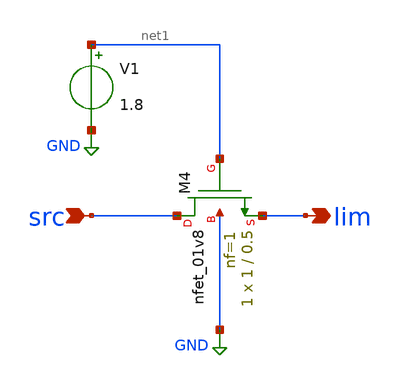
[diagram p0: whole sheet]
** sch_path: xschem/limb.sch
**.subckt limb src lim
*.ipin src
*.opin lim
XM4 src net1 lim GND sky130_fd_pr__nfet_01v8 L=0.5 W=1 nf=1 ad='int((nf+1)/2) * W/nf * 0.29' as='int((nf+2)/2) * W/nf * 0.29'
+ pd='2*int((nf+1)/2) * (W/nf + 0.29)' ps='2*int((nf+2)/2) * (W/nf + 0.29)' nrd='0.29 / W' nrs='0.29 / W'
+ sa=0 sb=0 sd=0 mult=1 m=1
V1 net1 GND 1.8
**.ends
.GLOBAL GND
.end
